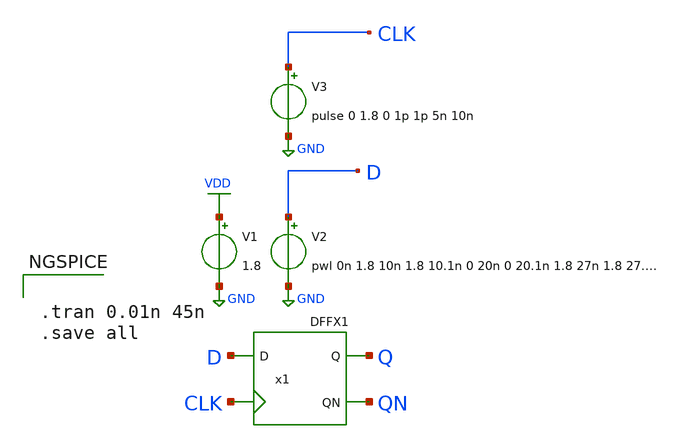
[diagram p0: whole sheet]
** sch_path: lib/xschem/test_DFFX1.sch
**.subckt test_DFFX1
V2 D GND pwl 0n 1.8 10n 1.8 10.1n 0 20n 0 20.1n 1.8 27n 1.8 27.1n 0 34n 0 34.1n 1.8
V1 VDD GND 1.8
V3 CLK GND pulse 0 1.8 0 1p 1p 5n 10n
x1 Q QN D CLK VDD GND DFFX1
**** begin user architecture code

.lib $::SKYWATER_MODELS/sky130.lib.spice tt


**** end user architecture code
**.ends
.GLOBAL VDD
.GLOBAL GND
**** begin user architecture code


.tran 0.01n 45n
.save all


**** end user architecture code
.end
